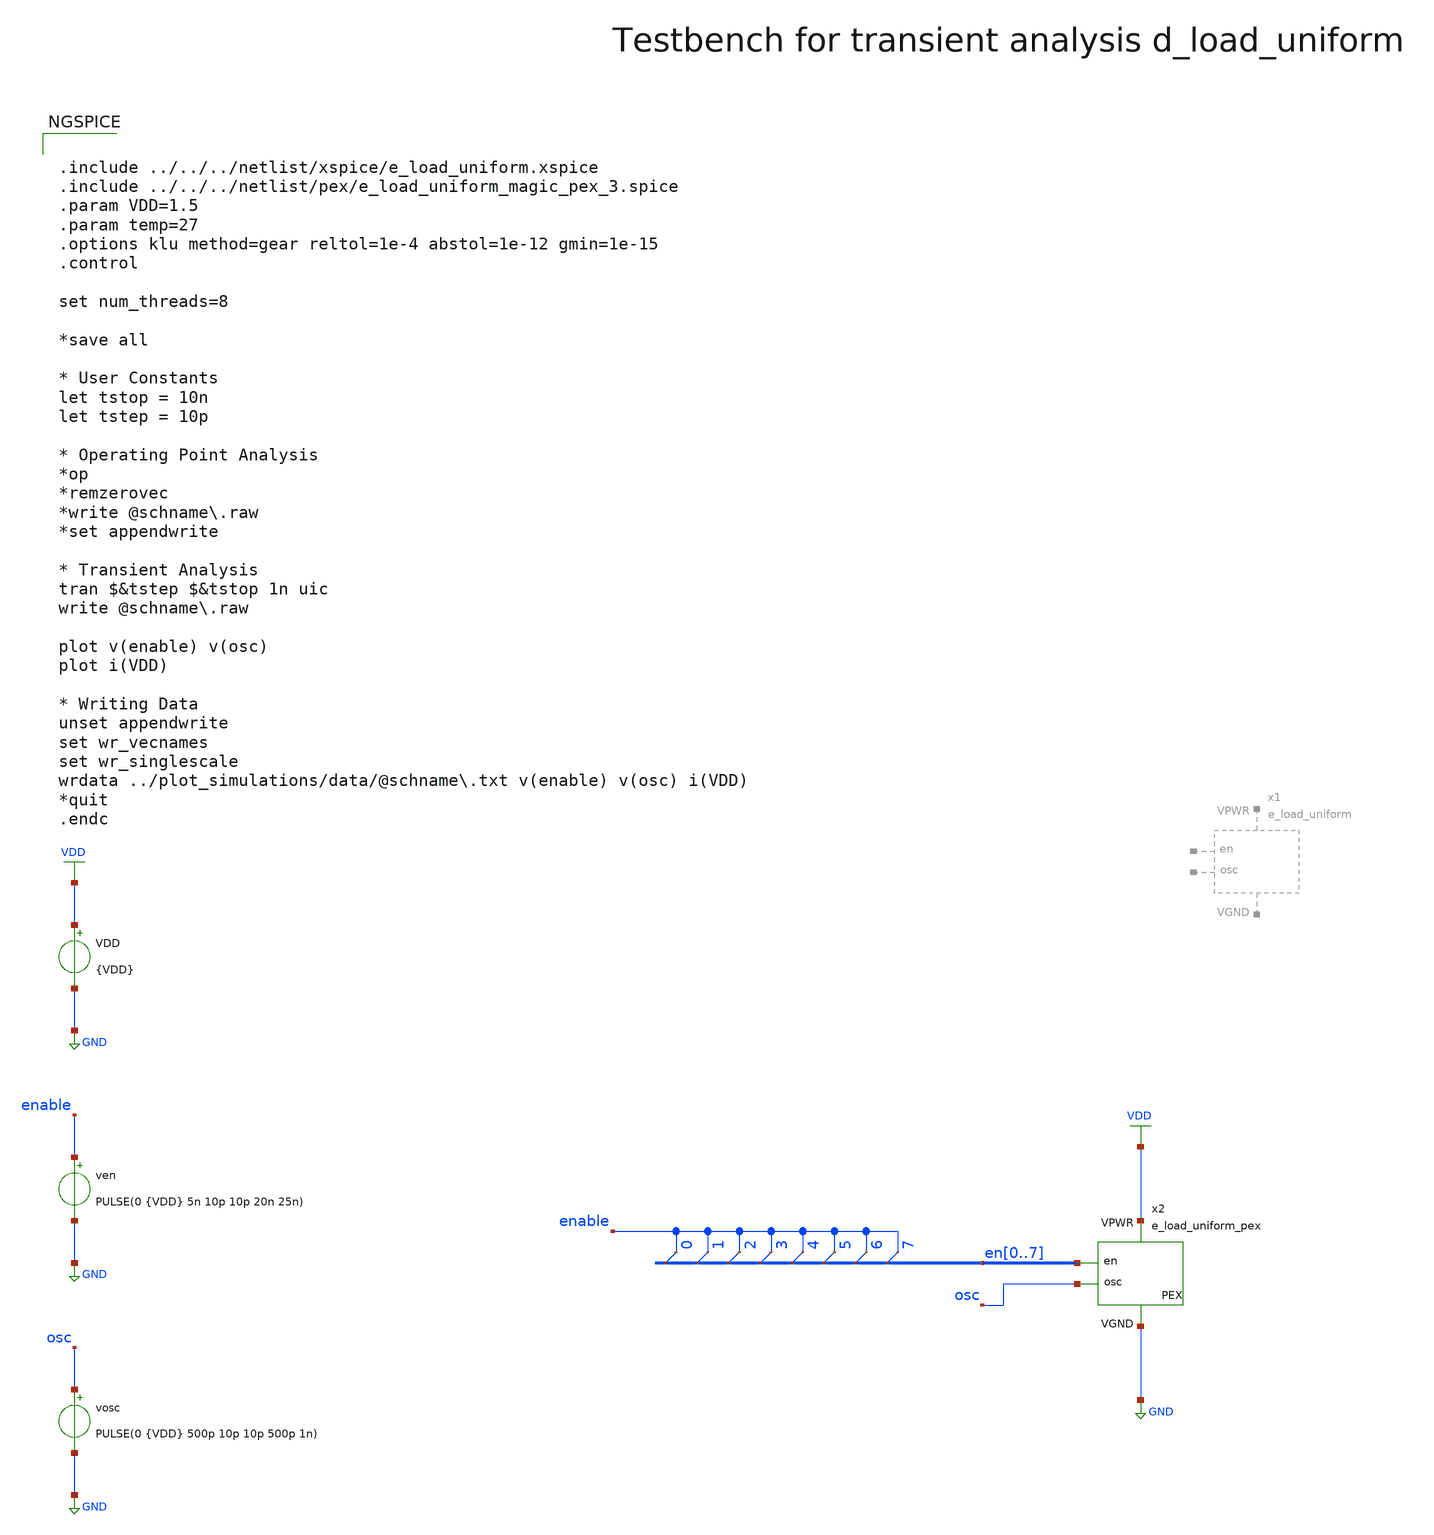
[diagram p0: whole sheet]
** sch_path: macros/heichips26_digital_project/macros/e_load_uniform/testbenches/xschem/e_load_uniform_tb_tran.sch
**.subckt e_load_uniform_tb_tran
VDD VDD GND {VDD}
ven enable GND PULSE(0 {VDD} 5n 10p 10p 20n 25n)
x2 VDD GND osc en0 en1 en2 en3 en4 en5 en6 en7 e_load_uniform_pex
vosc osc GND PULSE(0 {VDD} 500p 10p 10p 500p 1n)
* tap: en[0..7] --> en1
* tap: en[0..7] --> en1
* tap: en[0..7] --> en1
* tap: en[0..7] --> en1
* tap: en[0..7] --> en1
* tap: en[0..7] --> en1
* tap: en[0..7] --> en1
* tap: en[0..7] --> en1
**** begin user architecture code


.include ../../../netlist/xspice/e_load_uniform.xspice
.include ../../../netlist/pex/e_load_uniform_magic_pex_3.spice
.param VDD=1.5
.param temp=27
.options klu method=gear reltol=1e-4 abstol=1e-12 gmin=1e-15
.control

set num_threads=8

*save all

* User Constants
let tstop = 10n
let tstep = 10p

* Operating Point Analysis
*op
*remzerovec
*write @schname\.raw
*set appendwrite

* Transient Analysis
tran $&tstep $&tstop 1n uic
write @schname\.raw

plot v(enable) v(osc)
plot i(VDD)

* Writing Data
unset appendwrite
set wr_vecnames
set wr_singlescale
wrdata ../plot_simulations/data/@schname\.txt v(enable) v(osc) i(VDD)
*quit
.endc


.lib cornerMOSlv.lib mos_tt
.lib cornerMOShv.lib mos_tt
.lib cornerRES.lib res_typ
.lib cornerDIO.lib dio_tt

**** end user architecture code
**.ends
.GLOBAL GND
.GLOBAL VDD
.end
